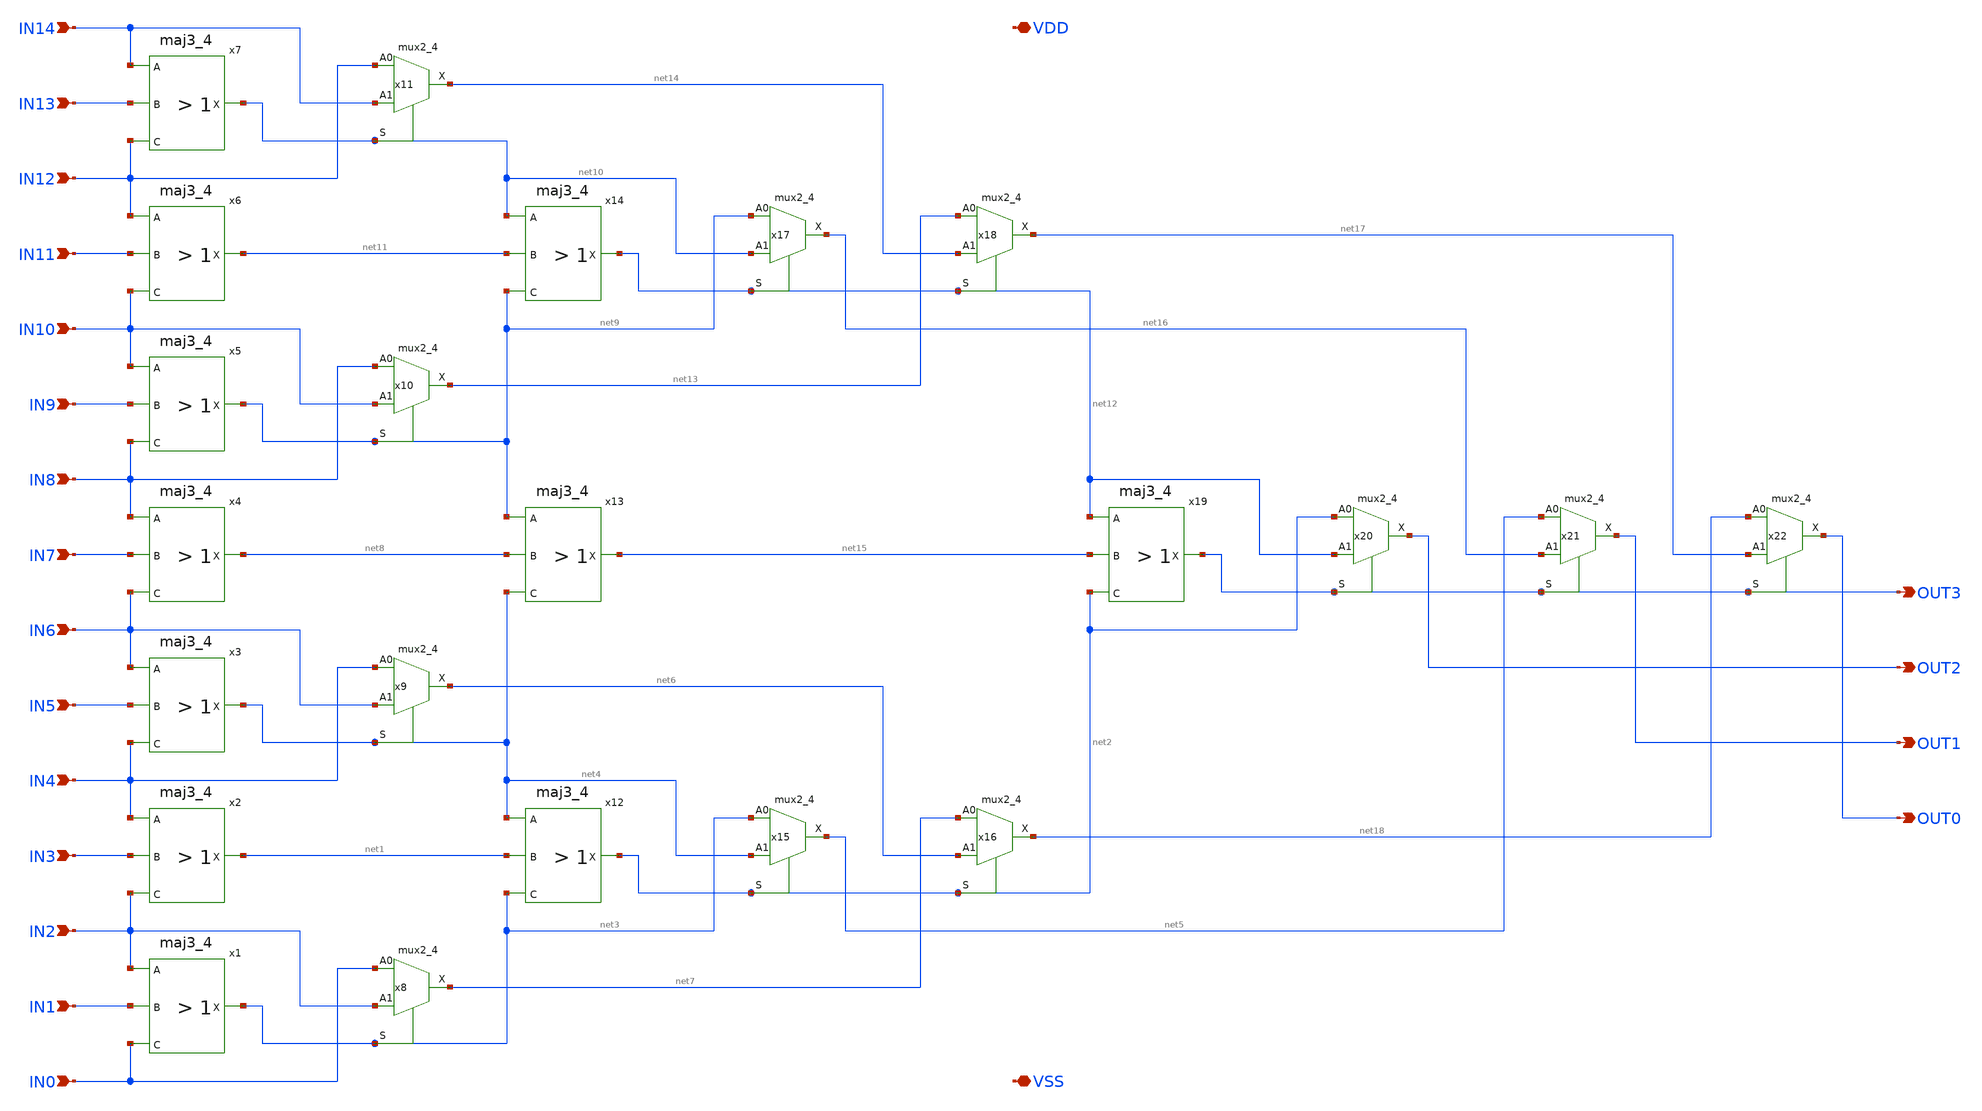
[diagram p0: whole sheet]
** sch_path: xschem/encoder_tree.sch
**.subckt encoder_tree IN0 IN1 IN2 IN3 IN4 IN5 IN6 IN7 IN8 IN9 IN10 IN11 IN12 IN13 IN14 OUT0 OUT1
*+ OUT2 OUT3 VDD VSS
*.ipin IN0
*.ipin IN1
*.ipin IN2
*.ipin IN3
*.ipin IN4
*.ipin IN5
*.ipin IN6
*.ipin IN7
*.ipin IN8
*.ipin IN9
*.ipin IN10
*.ipin IN11
*.ipin IN12
*.ipin IN13
*.ipin IN14
*.opin OUT0
*.opin OUT1
*.opin OUT2
*.opin OUT3
*.iopin VDD
*.iopin VSS
x1 IN2 IN1 IN0 VSS VSS VDD VDD net3 sky130_fd_sc_hd__maj3_4
x2 IN4 IN3 IN2 VSS VSS VDD VDD net1 sky130_fd_sc_hd__maj3_4
x3 IN6 IN5 IN4 VSS VSS VDD VDD net4 sky130_fd_sc_hd__maj3_4
x4 IN8 IN7 IN6 VSS VSS VDD VDD net8 sky130_fd_sc_hd__maj3_4
x5 IN10 IN9 IN8 VSS VSS VDD VDD net9 sky130_fd_sc_hd__maj3_4
x6 IN12 IN11 IN10 VSS VSS VDD VDD net11 sky130_fd_sc_hd__maj3_4
x7 IN14 IN13 IN12 VSS VSS VDD VDD net10 sky130_fd_sc_hd__maj3_4
x8 IN0 IN2 net3 VSS VSS VDD VDD net7 sky130_fd_sc_hd__mux2_4
x9 IN4 IN6 net4 VSS VSS VDD VDD net6 sky130_fd_sc_hd__mux2_4
x10 IN8 IN10 net9 VSS VSS VDD VDD net13 sky130_fd_sc_hd__mux2_4
x11 IN12 IN14 net10 VSS VSS VDD VDD net14 sky130_fd_sc_hd__mux2_4
x12 net4 net1 net3 VSS VSS VDD VDD net2 sky130_fd_sc_hd__maj3_4
x13 net9 net8 net4 VSS VSS VDD VDD net15 sky130_fd_sc_hd__maj3_4
x14 net10 net11 net9 VSS VSS VDD VDD net12 sky130_fd_sc_hd__maj3_4
x15 net3 net4 net2 VSS VSS VDD VDD net5 sky130_fd_sc_hd__mux2_4
x16 net7 net6 net2 VSS VSS VDD VDD net18 sky130_fd_sc_hd__mux2_4
x17 net9 net10 net12 VSS VSS VDD VDD net16 sky130_fd_sc_hd__mux2_4
x18 net13 net14 net12 VSS VSS VDD VDD net17 sky130_fd_sc_hd__mux2_4
x19 net12 net15 net2 VSS VSS VDD VDD OUT3 sky130_fd_sc_hd__maj3_4
x20 net2 net12 OUT3 VSS VSS VDD VDD OUT2 sky130_fd_sc_hd__mux2_4
x21 net5 net16 OUT3 VSS VSS VDD VDD OUT1 sky130_fd_sc_hd__mux2_4
x22 net18 net17 OUT3 VSS VSS VDD VDD OUT0 sky130_fd_sc_hd__mux2_4
**.ends
.end
